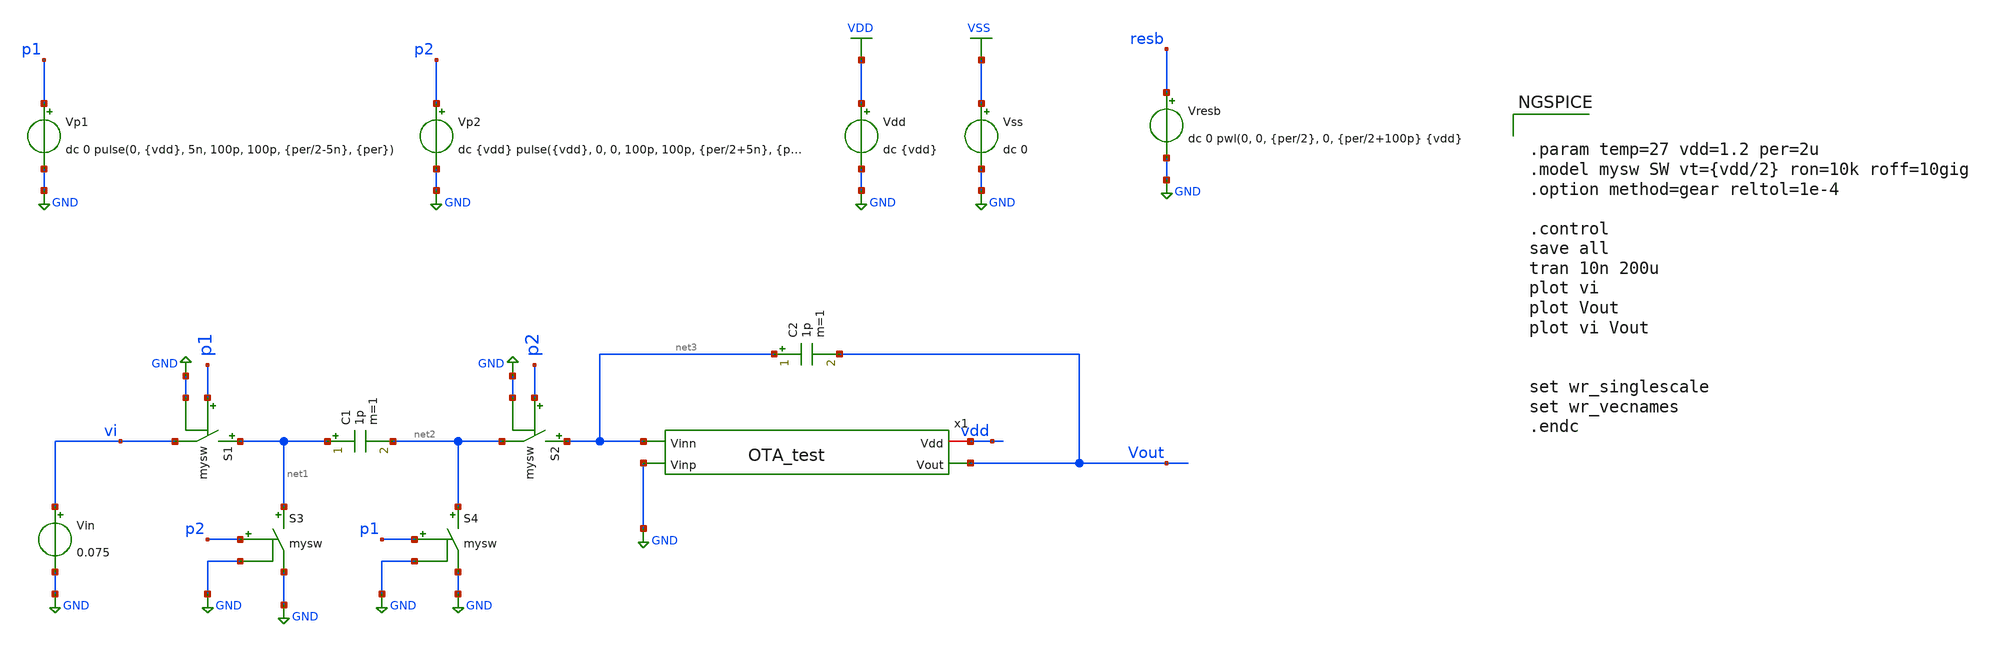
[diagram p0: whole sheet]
** sch_path: Xschem/OTA_Integrator.sch
**.subckt OTA_Integrator
Vp1 p1 GND dc 0 pulse(0, {vdd}, 5n, 100p, 100p, {per/2-5n}, {per})
Vp2 p2 GND dc {vdd} pulse({vdd}, 0, 0, 100p, 100p, {per/2+5n}, {per})
Vdd VDD GND dc {vdd}
Vss VSS GND dc 0
S1 net1 vi p1 GND mysw
Vin vi GND 0.075
C1 net1 net2 1p m=1
S2 net3 net2 p2 GND mysw
S3 net1 GND p2 GND mysw
S4 net2 GND p1 GND mysw
x1 vdd Vout net3 GND OTA_test
C2 net3 Vout 1p m=1
Vresb resb GND dc 0 pwl(0, 0, {per/2}, 0, {per/2+100p} {vdd}
**** begin user architecture code

.lib $::SG13G2_MODELS/cornerMOSlv.lib mos_tt
.lib $::SG13G2_MODELS/cornerRES.lib res_typ
.inc /foss/pdks/sg13g2/libs.ref/sg13g2_stdcell/spice/sg13g2_stdcell.spice



.param temp=27 vdd=1.2 per=2u
.model mysw SW vt={vdd/2} ron=10k roff=10gig
.option method=gear reltol=1e-4

.control
save all
tran 10n 200u
plot vi
plot Vout
plot vi Vout


set wr_singlescale
set wr_vecnames
.endc


**** end user architecture code
**.ends

* expanding   symbol:  OTA_test.sym # of pins=4
** sym_path: Xschem/OTA_test.sym
** sch_path: Xschem/OTA_test.sch
.subckt OTA_test Vdd Vout Vinn Vinp
*.opin Vout
*.iopin Vdd
*.ipin Vinp
*.ipin Vinn
I_basis Vdd net3 20u
XM1 net1 Vinp net2 GND sg13_lv_nmos w=2u l=5u ng=1 m=1 mm_ok=1
XM5 net2 net3 GND GND sg13_lv_nmos w=0.5u l=5u ng=1 m=1 mm_ok=1
XM6 net3 net3 GND GND sg13_lv_nmos w=2.5u l=5u ng=5 m=1 mm_ok=1
XM4 Vout net1 Vdd Vdd sg13_lv_pmos w=1.5u l=5u ng=1 m=1 mm_ok=1
XM3 net1 net1 Vdd Vdd sg13_lv_pmos w=1.5u l=5u ng=1 m=1 mm_ok=1
XM2 Vout Vinn net2 GND sg13_lv_nmos w=2u l=5u ng=1 m=1 mm_ok=1
.ends

.GLOBAL GND
.GLOBAL VDD
.GLOBAL VSS
.end
